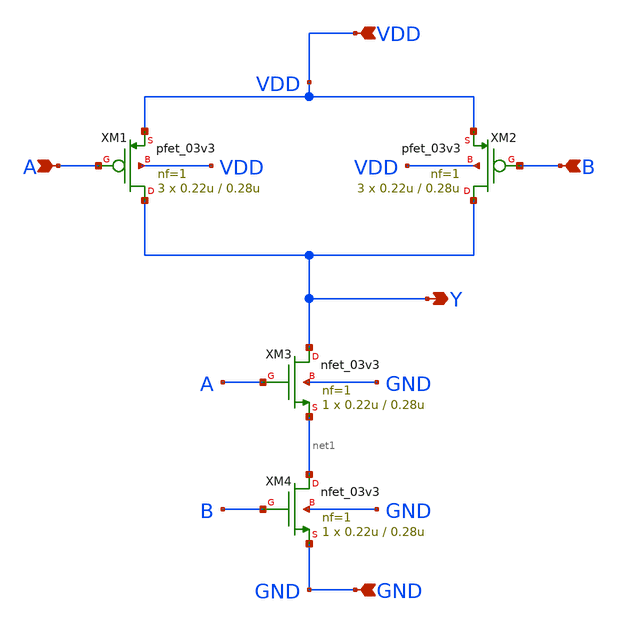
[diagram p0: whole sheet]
** sch_path: PFD/NAND.sch
**.subckt NAND Y GND VDD A B
*.opin Y
*.ipin GND
*.ipin VDD
*.ipin A
*.ipin B
XM1 Y A net2 VDD pfet_03v3 L=0.28u W=0.22u nf=1 ad='int((nf+1)/2) * W/nf * 0.18u' as='int((nf+2)/2) * W/nf * 0.18u'
+ pd='2*int((nf+1)/2) * (W/nf + 0.18u)' ps='2*int((nf+2)/2) * (W/nf + 0.18u)' nrd='0.18u / W' nrs='0.18u / W'
+ sa=0 sb=0 sd=0 m=3
XM3 Y A net1 GND nfet_03v3 L=0.28u W=0.22u nf=1 ad='int((nf+1)/2) * W/nf * 0.18u' as='int((nf+2)/2) * W/nf * 0.18u'
+ pd='2*int((nf+1)/2) * (W/nf + 0.18u)' ps='2*int((nf+2)/2) * (W/nf + 0.18u)' nrd='0.18u / W' nrs='0.18u / W'
+ sa=0 sb=0 sd=0 m=1
XM4 net1 B GND GND nfet_03v3 L=0.28u W=0.22u nf=1 ad='int((nf+1)/2) * W/nf * 0.18u' as='int((nf+2)/2) * W/nf * 0.18u'
+ pd='2*int((nf+1)/2) * (W/nf + 0.18u)' ps='2*int((nf+2)/2) * (W/nf + 0.18u)' nrd='0.18u / W' nrs='0.18u / W'
+ sa=0 sb=0 sd=0 m=1
XM2 Y B net3 VDD pfet_03v3 L=0.28u W=0.22u nf=1 ad='int((nf+1)/2) * W/nf * 0.18u' as='int((nf+2)/2) * W/nf * 0.18u'
+ pd='2*int((nf+1)/2) * (W/nf + 0.18u)' ps='2*int((nf+2)/2) * (W/nf + 0.18u)' nrd='0.18u / W' nrs='0.18u / W'
+ sa=0 sb=0 sd=0 m=3
**.ends
.end
